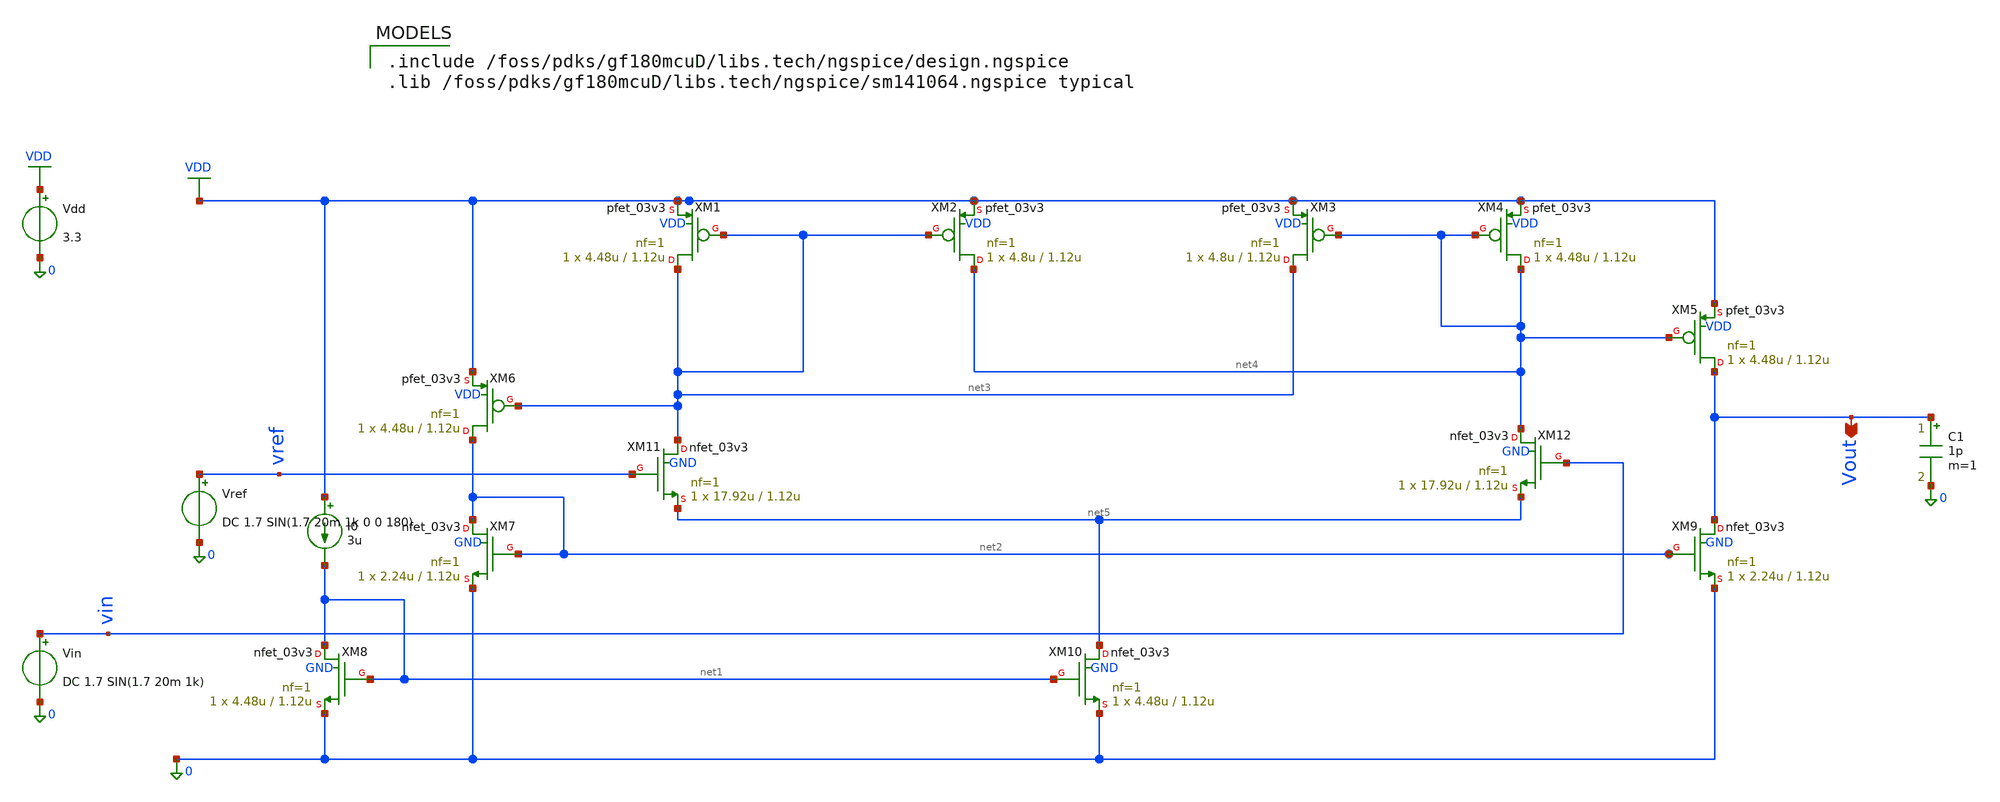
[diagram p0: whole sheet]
** sch_path: comparator/schematic-design/coc_sim2.sch
**.subckt coc_sim2 Vout
*.opin Vout
XM1 net3 net3 VDD VDD pfet_03v3 L=1.12u W=4.48u nf=1 ad='int((nf+1)/2) * W/nf * 0.18u' as='int((nf+2)/2) * W/nf * 0.18u'
+ pd='2*int((nf+1)/2) * (W/nf + 0.18u)' ps='2*int((nf+2)/2) * (W/nf + 0.18u)' nrd='0.18u / W' nrs='0.18u / W'
+ sa=0 sb=0 sd=0 m=1 par=1
XM2 net4 net3 VDD VDD pfet_03v3 L=1.12u W=4.8u nf=1 ad='int((nf+1)/2) * W/nf * 0.18u' as='int((nf+2)/2) * W/nf * 0.18u'
+ pd='2*int((nf+1)/2) * (W/nf + 0.18u)' ps='2*int((nf+2)/2) * (W/nf + 0.18u)' nrd='0.18u / W' nrs='0.18u / W'
+ sa=0 sb=0 sd=0 m=1 par=1
XM3 net3 net4 VDD VDD pfet_03v3 L=1.12u W=4.8u nf=1 ad='int((nf+1)/2) * W/nf * 0.18u' as='int((nf+2)/2) * W/nf * 0.18u'
+ pd='2*int((nf+1)/2) * (W/nf + 0.18u)' ps='2*int((nf+2)/2) * (W/nf + 0.18u)' nrd='0.18u / W' nrs='0.18u / W'
+ sa=0 sb=0 sd=0 m=1 par=1
XM4 net4 net4 VDD VDD pfet_03v3 L=1.12u W=4.48u nf=1 ad='int((nf+1)/2) * W/nf * 0.18u' as='int((nf+2)/2) * W/nf * 0.18u'
+ pd='2*int((nf+1)/2) * (W/nf + 0.18u)' ps='2*int((nf+2)/2) * (W/nf + 0.18u)' nrd='0.18u / W' nrs='0.18u / W'
+ sa=0 sb=0 sd=0 m=1 par=1
XM5 Vout net4 VDD VDD pfet_03v3 L=1.12u W=4.48u nf=1 ad='int((nf+1)/2) * W/nf * 0.18u' as='int((nf+2)/2) * W/nf * 0.18u'
+ pd='2*int((nf+1)/2) * (W/nf + 0.18u)' ps='2*int((nf+2)/2) * (W/nf + 0.18u)' nrd='0.18u / W' nrs='0.18u / W'
+ sa=0 sb=0 sd=0 m=1 par=1
XM6 net2 net3 VDD VDD pfet_03v3 L=1.12u W=4.48u nf=1 ad='int((nf+1)/2) * W/nf * 0.18u' as='int((nf+2)/2) * W/nf * 0.18u'
+ pd='2*int((nf+1)/2) * (W/nf + 0.18u)' ps='2*int((nf+2)/2) * (W/nf + 0.18u)' nrd='0.18u / W' nrs='0.18u / W'
+ sa=0 sb=0 sd=0 m=1 par=1
XM7 net2 net2 0 GND nfet_03v3 L=1.12u W=2.24u nf=1 ad='int((nf+1)/2) * W/nf * 0.18u' as='int((nf+2)/2) * W/nf * 0.18u'
+ pd='2*int((nf+1)/2) * (W/nf + 0.18u)' ps='2*int((nf+2)/2) * (W/nf + 0.18u)' nrd='0.18u / W' nrs='0.18u / W'
+ sa=0 sb=0 sd=0 m=1 par=1
XM8 net1 net1 0 GND nfet_03v3 L=1.12u W=4.48u nf=1 ad='int((nf+1)/2) * W/nf * 0.18u' as='int((nf+2)/2) * W/nf * 0.18u'
+ pd='2*int((nf+1)/2) * (W/nf + 0.18u)' ps='2*int((nf+2)/2) * (W/nf + 0.18u)' nrd='0.18u / W' nrs='0.18u / W'
+ sa=0 sb=0 sd=0 m=1 par=1
XM9 Vout net2 0 GND nfet_03v3 L=1.12u W=2.24u nf=1 ad='int((nf+1)/2) * W/nf * 0.18u' as='int((nf+2)/2) * W/nf * 0.18u'
+ pd='2*int((nf+1)/2) * (W/nf + 0.18u)' ps='2*int((nf+2)/2) * (W/nf + 0.18u)' nrd='0.18u / W' nrs='0.18u / W'
+ sa=0 sb=0 sd=0 m=1 par=1
XM10 net5 net1 0 GND nfet_03v3 L=1.12u W=4.48u nf=1 ad='int((nf+1)/2) * W/nf * 0.18u' as='int((nf+2)/2) * W/nf * 0.18u'
+ pd='2*int((nf+1)/2) * (W/nf + 0.18u)' ps='2*int((nf+2)/2) * (W/nf + 0.18u)' nrd='0.18u / W' nrs='0.18u / W'
+ sa=0 sb=0 sd=0 m=1 par=1
XM11 net3 vref net5 GND nfet_03v3 L=1.12u W=17.92u nf=1 ad='int((nf+1)/2) * W/nf * 0.18u' as='int((nf+2)/2) * W/nf * 0.18u'
+ pd='2*int((nf+1)/2) * (W/nf + 0.18u)' ps='2*int((nf+2)/2) * (W/nf + 0.18u)' nrd='0.18u / W' nrs='0.18u / W'
+ sa=0 sb=0 sd=0 m=1 par=1
XM12 net4 vin net5 GND nfet_03v3 L=1.12u W=17.92u nf=1 ad='int((nf+1)/2) * W/nf * 0.18u' as='int((nf+2)/2) * W/nf * 0.18u'
+ pd='2*int((nf+1)/2) * (W/nf + 0.18u)' ps='2*int((nf+2)/2) * (W/nf + 0.18u)' nrd='0.18u / W' nrs='0.18u / W'
+ sa=0 sb=0 sd=0 m=1 par=1
I0 VDD net1 3u
Vref vref 0 DC 1.7 SIN(1.7 20m 1k 0 0 180)
Vin vin 0 DC 1.7 SIN(1.7 20m 1k)

Vdd VDD 0 3.3
C1 Vout 0 1p m=1
**** begin user architecture code

.include /foss/pdks/gf180mcuD/libs.tech/ngspice/design.ngspice
.lib /foss/pdks/gf180mcuD/libs.tech/ngspice/sm141064.ngspice typical


.control
save v(vin) v(vout)

dc Vin 1.80 1.60 -0.1m
plot v(vout)

.endc


**** end user architecture code
**.ends
.GLOBAL VDD
.end
